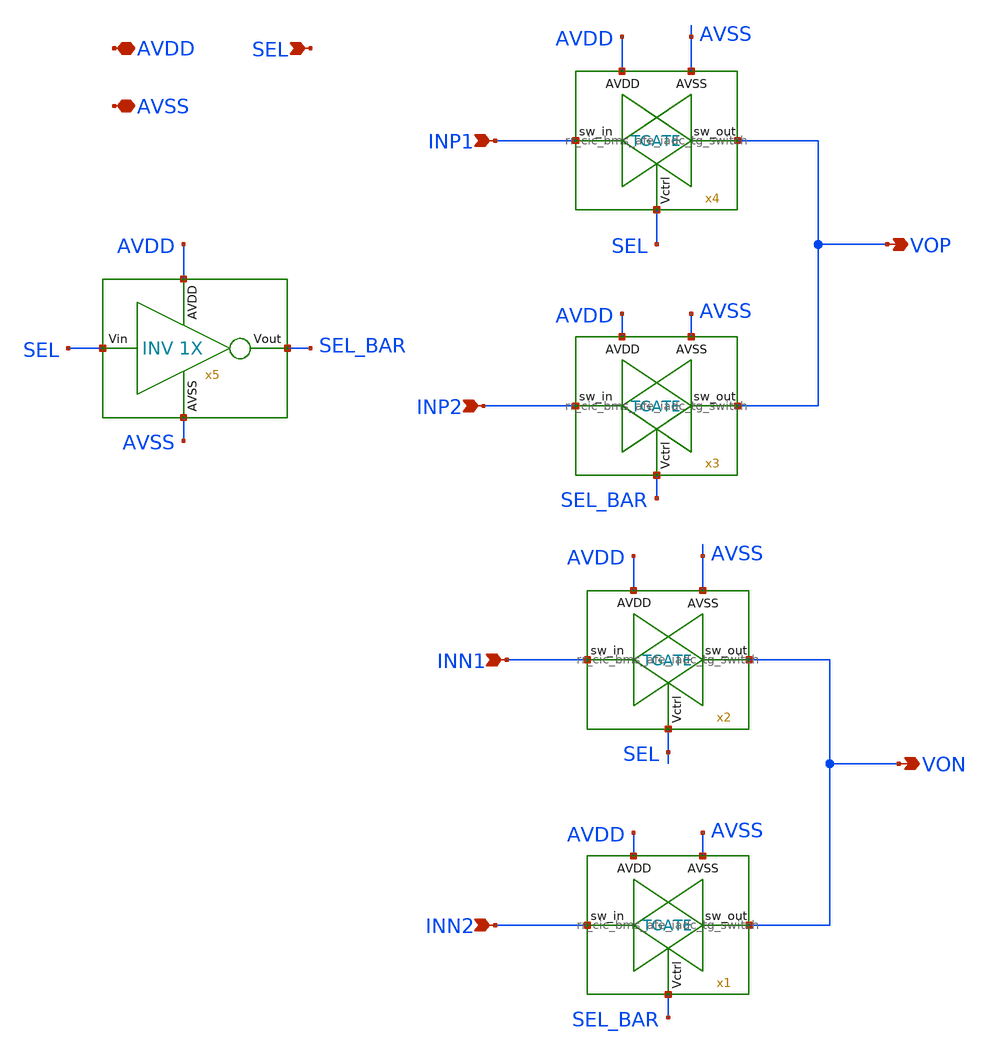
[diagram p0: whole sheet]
** sch_path: design/schematics/MUX/pkr_cic_bms_afe_mux_4x2.sch
**.subckt pkr_cic_bms_afe_mux_4x2 INP1 INP2 INN1 INN2 VOP VON SEL AVDD AVSS
*.ipin INP1
*.ipin INP2
*.ipin INN1
*.ipin INN2
*.opin VOP
*.opin VON
*.ipin SEL
*.iopin AVDD
*.iopin AVSS
x1 AVDD SEL_BAR INN2 VON AVSS rr_cic_bms_afe_iadc_tg_switch
x2 AVDD SEL INN1 VON AVSS rr_cic_bms_afe_iadc_tg_switch
x3 AVDD SEL_BAR INP2 VOP AVSS rr_cic_bms_afe_iadc_tg_switch
x4 AVDD SEL INP1 VOP AVSS rr_cic_bms_afe_iadc_tg_switch
x5 AVDD SEL_BAR SEL AVSS sa_cic_bms_afe_iadc_quantizer_inv1x
**.ends
.end
